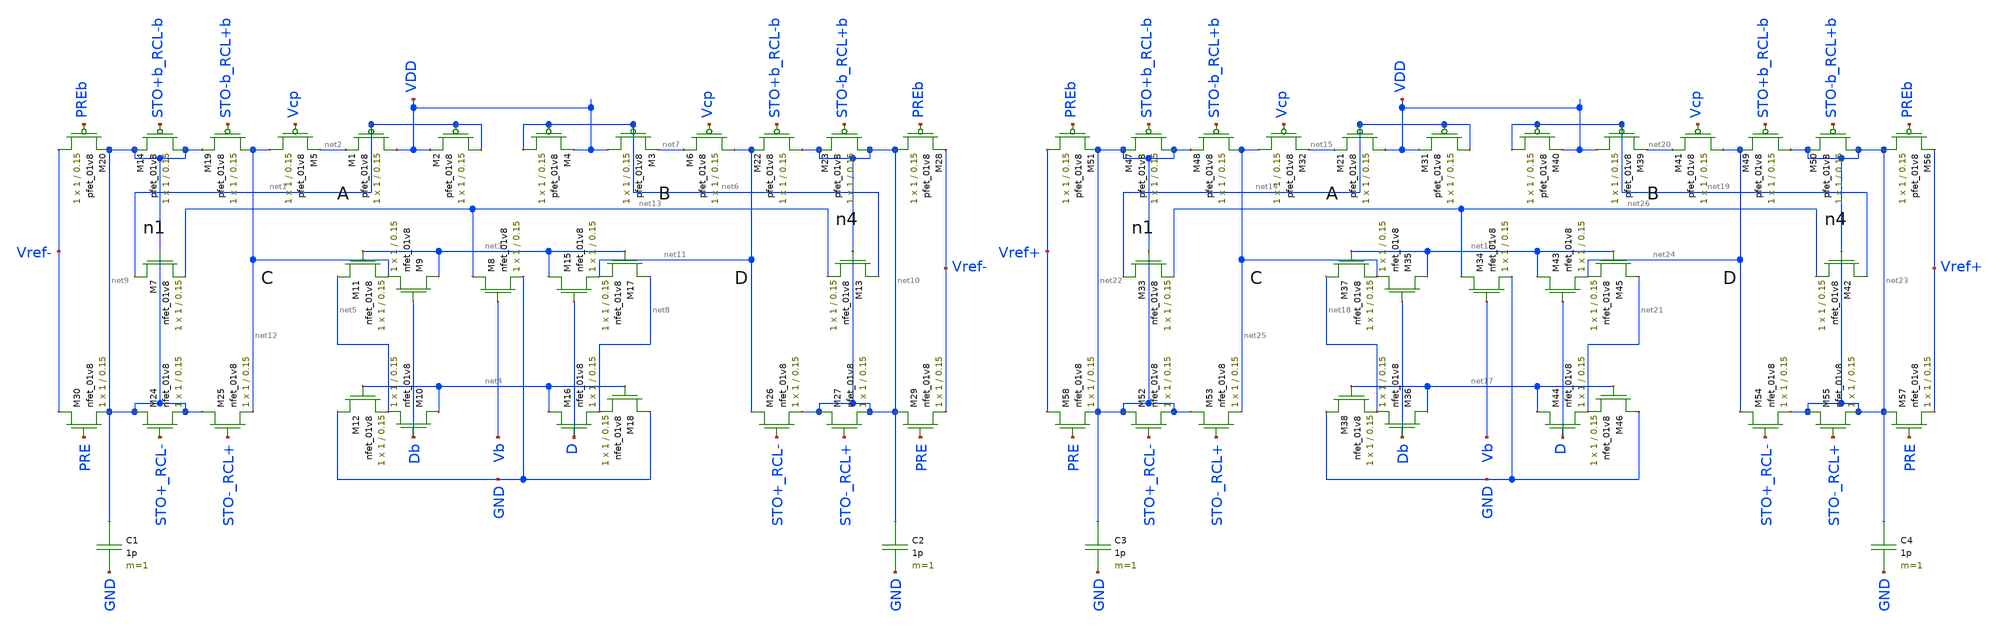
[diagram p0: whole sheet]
** sch_path: OTAs_lds.sch
**.subckt OTAs_lds
XM1 VDD net1 net2 VDD sky130_fd_pr__pfet_01v8 L=0.15 W=1 nf=1 ad='int((nf+1)/2) * W/nf * 0.29' as='int((nf+2)/2) * W/nf * 0.29'
+ pd='2*int((nf+1)/2) * (W/nf + 0.29)' ps='2*int((nf+2)/2) * (W/nf + 0.29)' nrd='0.29 / W' nrs='0.29 / W'
+ sa=0 sb=0 sd=0 mult=1 m=1
XM2 net1 net1 VDD VDD sky130_fd_pr__pfet_01v8 L=0.15 W=1 nf=1 ad='int((nf+1)/2) * W/nf * 0.29' as='int((nf+2)/2) * W/nf * 0.29'
+ pd='2*int((nf+1)/2) * (W/nf + 0.29)' ps='2*int((nf+2)/2) * (W/nf + 0.29)' nrd='0.29 / W' nrs='0.29 / W'
+ sa=0 sb=0 sd=0 mult=1 m=1
XM5 net12 Vcp net2 VDD sky130_fd_pr__pfet_01v8 L=0.15 W=1 nf=1 ad='int((nf+1)/2) * W/nf * 0.29' as='int((nf+2)/2) * W/nf * 0.29'
+ pd='2*int((nf+1)/2) * (W/nf + 0.29)' ps='2*int((nf+2)/2) * (W/nf + 0.29)' nrd='0.29 / W' nrs='0.29 / W'
+ sa=0 sb=0 sd=0 mult=1 m=1
XM7 net1 net9 net13 GND sky130_fd_pr__nfet_01v8 L=0.15 W=1 nf=1 ad='int((nf+1)/2) * W/nf * 0.29' as='int((nf+2)/2) * W/nf * 0.29'
+ pd='2*int((nf+1)/2) * (W/nf + 0.29)' ps='2*int((nf+2)/2) * (W/nf + 0.29)' nrd='0.29 / W' nrs='0.29 / W'
+ sa=0 sb=0 sd=0 mult=1 m=1
XM8 net13 Vb GND GND sky130_fd_pr__nfet_01v8 L=0.15 W=1 nf=1 ad='int((nf+1)/2) * W/nf * 0.29' as='int((nf+2)/2) * W/nf * 0.29'
+ pd='2*int((nf+1)/2) * (W/nf + 0.29)' ps='2*int((nf+2)/2) * (W/nf + 0.29)' nrd='0.29 / W' nrs='0.29 / W'
+ sa=0 sb=0 sd=0 mult=1 m=1
XM9 net3 Db net12 GND sky130_fd_pr__nfet_01v8 L=0.15 W=1 nf=1 ad='int((nf+1)/2) * W/nf * 0.29' as='int((nf+2)/2) * W/nf * 0.29'
+ pd='2*int((nf+1)/2) * (W/nf + 0.29)' ps='2*int((nf+2)/2) * (W/nf + 0.29)' nrd='0.29 / W' nrs='0.29 / W'
+ sa=0 sb=0 sd=0 mult=1 m=1
XM10 net4 Db net5 GND sky130_fd_pr__nfet_01v8 L=0.15 W=1 nf=1 ad='int((nf+1)/2) * W/nf * 0.29' as='int((nf+2)/2) * W/nf * 0.29'
+ pd='2*int((nf+1)/2) * (W/nf + 0.29)' ps='2*int((nf+2)/2) * (W/nf + 0.29)' nrd='0.29 / W' nrs='0.29 / W'
+ sa=0 sb=0 sd=0 mult=1 m=1
XM11 net5 net3 net12 GND sky130_fd_pr__nfet_01v8 L=0.15 W=1 nf=1 ad='int((nf+1)/2) * W/nf * 0.29' as='int((nf+2)/2) * W/nf * 0.29'
+ pd='2*int((nf+1)/2) * (W/nf + 0.29)' ps='2*int((nf+2)/2) * (W/nf + 0.29)' nrd='0.29 / W' nrs='0.29 / W'
+ sa=0 sb=0 sd=0 mult=1 m=1
XM12 GND net4 net5 GND sky130_fd_pr__nfet_01v8 L=0.15 W=1 nf=1 ad='int((nf+1)/2) * W/nf * 0.29' as='int((nf+2)/2) * W/nf * 0.29'
+ pd='2*int((nf+1)/2) * (W/nf + 0.29)' ps='2*int((nf+2)/2) * (W/nf + 0.29)' nrd='0.29 / W' nrs='0.29 / W'
+ sa=0 sb=0 sd=0 mult=1 m=1
XM3 VDD net6 net7 VDD sky130_fd_pr__pfet_01v8 L=0.15 W=1 nf=1 ad='int((nf+1)/2) * W/nf * 0.29' as='int((nf+2)/2) * W/nf * 0.29'
+ pd='2*int((nf+1)/2) * (W/nf + 0.29)' ps='2*int((nf+2)/2) * (W/nf + 0.29)' nrd='0.29 / W' nrs='0.29 / W'
+ sa=0 sb=0 sd=0 mult=1 m=1
XM4 net6 net6 VDD VDD sky130_fd_pr__pfet_01v8 L=0.15 W=1 nf=1 ad='int((nf+1)/2) * W/nf * 0.29' as='int((nf+2)/2) * W/nf * 0.29'
+ pd='2*int((nf+1)/2) * (W/nf + 0.29)' ps='2*int((nf+2)/2) * (W/nf + 0.29)' nrd='0.29 / W' nrs='0.29 / W'
+ sa=0 sb=0 sd=0 mult=1 m=1
XM6 net11 Vcp net7 VDD sky130_fd_pr__pfet_01v8 L=0.15 W=1 nf=1 ad='int((nf+1)/2) * W/nf * 0.29' as='int((nf+2)/2) * W/nf * 0.29'
+ pd='2*int((nf+1)/2) * (W/nf + 0.29)' ps='2*int((nf+2)/2) * (W/nf + 0.29)' nrd='0.29 / W' nrs='0.29 / W'
+ sa=0 sb=0 sd=0 mult=1 m=1
XM13 net6 net10 net13 GND sky130_fd_pr__nfet_01v8 L=0.15 W=1 nf=1 ad='int((nf+1)/2) * W/nf * 0.29' as='int((nf+2)/2) * W/nf * 0.29'
+ pd='2*int((nf+1)/2) * (W/nf + 0.29)' ps='2*int((nf+2)/2) * (W/nf + 0.29)' nrd='0.29 / W' nrs='0.29 / W'
+ sa=0 sb=0 sd=0 mult=1 m=1
XM15 net3 D net11 GND sky130_fd_pr__nfet_01v8 L=0.15 W=1 nf=1 ad='int((nf+1)/2) * W/nf * 0.29' as='int((nf+2)/2) * W/nf * 0.29'
+ pd='2*int((nf+1)/2) * (W/nf + 0.29)' ps='2*int((nf+2)/2) * (W/nf + 0.29)' nrd='0.29 / W' nrs='0.29 / W'
+ sa=0 sb=0 sd=0 mult=1 m=1
XM16 net4 D net8 GND sky130_fd_pr__nfet_01v8 L=0.15 W=1 nf=1 ad='int((nf+1)/2) * W/nf * 0.29' as='int((nf+2)/2) * W/nf * 0.29'
+ pd='2*int((nf+1)/2) * (W/nf + 0.29)' ps='2*int((nf+2)/2) * (W/nf + 0.29)' nrd='0.29 / W' nrs='0.29 / W'
+ sa=0 sb=0 sd=0 mult=1 m=1
XM17 net8 net3 net11 GND sky130_fd_pr__nfet_01v8 L=0.15 W=1 nf=1 ad='int((nf+1)/2) * W/nf * 0.29' as='int((nf+2)/2) * W/nf * 0.29'
+ pd='2*int((nf+1)/2) * (W/nf + 0.29)' ps='2*int((nf+2)/2) * (W/nf + 0.29)' nrd='0.29 / W' nrs='0.29 / W'
+ sa=0 sb=0 sd=0 mult=1 m=1
XM18 GND net4 net8 GND sky130_fd_pr__nfet_01v8 L=0.15 W=1 nf=1 ad='int((nf+1)/2) * W/nf * 0.29' as='int((nf+2)/2) * W/nf * 0.29'
+ pd='2*int((nf+1)/2) * (W/nf + 0.29)' ps='2*int((nf+2)/2) * (W/nf + 0.29)' nrd='0.29 / W' nrs='0.29 / W'
+ sa=0 sb=0 sd=0 mult=1 m=1
XM14 net9 STO+b_RCL-b net9 VDD sky130_fd_pr__pfet_01v8 L=0.15 W=1 nf=1 ad='int((nf+1)/2) * W/nf * 0.29'
+ as='int((nf+2)/2) * W/nf * 0.29' pd='2*int((nf+1)/2) * (W/nf + 0.29)' ps='2*int((nf+2)/2) * (W/nf + 0.29)'
+ nrd='0.29 / W' nrs='0.29 / W' sa=0 sb=0 sd=0 mult=1 m=1
XM19 net12 STO-b_RCL+b net9 VDD sky130_fd_pr__pfet_01v8 L=0.15 W=1 nf=1 ad='int((nf+1)/2) * W/nf * 0.29'
+ as='int((nf+2)/2) * W/nf * 0.29' pd='2*int((nf+1)/2) * (W/nf + 0.29)' ps='2*int((nf+2)/2) * (W/nf + 0.29)'
+ nrd='0.29 / W' nrs='0.29 / W' sa=0 sb=0 sd=0 mult=1 m=1
XM22 net10 STO+b_RCL-b net11 VDD sky130_fd_pr__pfet_01v8 L=0.15 W=1 nf=1 ad='int((nf+1)/2) * W/nf * 0.29'
+ as='int((nf+2)/2) * W/nf * 0.29' pd='2*int((nf+1)/2) * (W/nf + 0.29)' ps='2*int((nf+2)/2) * (W/nf + 0.29)'
+ nrd='0.29 / W' nrs='0.29 / W' sa=0 sb=0 sd=0 mult=1 m=1
XM23 net10 STO-b_RCL+b net10 VDD sky130_fd_pr__pfet_01v8 L=0.15 W=1 nf=1 ad='int((nf+1)/2) * W/nf * 0.29'
+ as='int((nf+2)/2) * W/nf * 0.29' pd='2*int((nf+1)/2) * (W/nf + 0.29)' ps='2*int((nf+2)/2) * (W/nf + 0.29)'
+ nrd='0.29 / W' nrs='0.29 / W' sa=0 sb=0 sd=0 mult=1 m=1
XM20 Vref- PREb net9 VDD sky130_fd_pr__pfet_01v8 L=0.15 W=1 nf=1 ad='int((nf+1)/2) * W/nf * 0.29' as='int((nf+2)/2) * W/nf * 0.29'
+ pd='2*int((nf+1)/2) * (W/nf + 0.29)' ps='2*int((nf+2)/2) * (W/nf + 0.29)' nrd='0.29 / W' nrs='0.29 / W'
+ sa=0 sb=0 sd=0 mult=1 m=1
XM24 net9 STO+_RCL- net9 GND sky130_fd_pr__nfet_01v8 L=0.15 W=1 nf=1 ad='int((nf+1)/2) * W/nf * 0.29'
+ as='int((nf+2)/2) * W/nf * 0.29' pd='2*int((nf+1)/2) * (W/nf + 0.29)' ps='2*int((nf+2)/2) * (W/nf + 0.29)'
+ nrd='0.29 / W' nrs='0.29 / W' sa=0 sb=0 sd=0 mult=1 m=1
XM25 net9 STO-_RCL+ net12 GND sky130_fd_pr__nfet_01v8 L=0.15 W=1 nf=1 ad='int((nf+1)/2) * W/nf * 0.29'
+ as='int((nf+2)/2) * W/nf * 0.29' pd='2*int((nf+1)/2) * (W/nf + 0.29)' ps='2*int((nf+2)/2) * (W/nf + 0.29)'
+ nrd='0.29 / W' nrs='0.29 / W' sa=0 sb=0 sd=0 mult=1 m=1
XM26 net11 STO+_RCL- net10 GND sky130_fd_pr__nfet_01v8 L=0.15 W=1 nf=1 ad='int((nf+1)/2) * W/nf * 0.29'
+ as='int((nf+2)/2) * W/nf * 0.29' pd='2*int((nf+1)/2) * (W/nf + 0.29)' ps='2*int((nf+2)/2) * (W/nf + 0.29)'
+ nrd='0.29 / W' nrs='0.29 / W' sa=0 sb=0 sd=0 mult=1 m=1
XM27 net10 STO-_RCL+ net10 GND sky130_fd_pr__nfet_01v8 L=0.15 W=1 nf=1 ad='int((nf+1)/2) * W/nf * 0.29'
+ as='int((nf+2)/2) * W/nf * 0.29' pd='2*int((nf+1)/2) * (W/nf + 0.29)' ps='2*int((nf+2)/2) * (W/nf + 0.29)'
+ nrd='0.29 / W' nrs='0.29 / W' sa=0 sb=0 sd=0 mult=1 m=1
XM28 net10 PREb Vref- VDD sky130_fd_pr__pfet_01v8 L=0.15 W=1 nf=1 ad='int((nf+1)/2) * W/nf * 0.29' as='int((nf+2)/2) * W/nf * 0.29'
+ pd='2*int((nf+1)/2) * (W/nf + 0.29)' ps='2*int((nf+2)/2) * (W/nf + 0.29)' nrd='0.29 / W' nrs='0.29 / W'
+ sa=0 sb=0 sd=0 mult=1 m=1
XM29 net10 PRE Vref- GND sky130_fd_pr__nfet_01v8 L=0.15 W=1 nf=1 ad='int((nf+1)/2) * W/nf * 0.29' as='int((nf+2)/2) * W/nf * 0.29'
+ pd='2*int((nf+1)/2) * (W/nf + 0.29)' ps='2*int((nf+2)/2) * (W/nf + 0.29)' nrd='0.29 / W' nrs='0.29 / W'
+ sa=0 sb=0 sd=0 mult=1 m=1
XM30 Vref- PRE net9 GND sky130_fd_pr__nfet_01v8 L=0.15 W=1 nf=1 ad='int((nf+1)/2) * W/nf * 0.29' as='int((nf+2)/2) * W/nf * 0.29'
+ pd='2*int((nf+1)/2) * (W/nf + 0.29)' ps='2*int((nf+2)/2) * (W/nf + 0.29)' nrd='0.29 / W' nrs='0.29 / W'
+ sa=0 sb=0 sd=0 mult=1 m=1
C1 net9 GND 1p m=1
C2 net10 GND 1p m=1
XM21 VDD net14 net15 VDD sky130_fd_pr__pfet_01v8 L=0.15 W=1 nf=1 ad='int((nf+1)/2) * W/nf * 0.29' as='int((nf+2)/2) * W/nf * 0.29'
+ pd='2*int((nf+1)/2) * (W/nf + 0.29)' ps='2*int((nf+2)/2) * (W/nf + 0.29)' nrd='0.29 / W' nrs='0.29 / W'
+ sa=0 sb=0 sd=0 mult=1 m=1
XM31 net14 net14 VDD VDD sky130_fd_pr__pfet_01v8 L=0.15 W=1 nf=1 ad='int((nf+1)/2) * W/nf * 0.29' as='int((nf+2)/2) * W/nf * 0.29'
+ pd='2*int((nf+1)/2) * (W/nf + 0.29)' ps='2*int((nf+2)/2) * (W/nf + 0.29)' nrd='0.29 / W' nrs='0.29 / W'
+ sa=0 sb=0 sd=0 mult=1 m=1
XM32 net25 Vcp net15 VDD sky130_fd_pr__pfet_01v8 L=0.15 W=1 nf=1 ad='int((nf+1)/2) * W/nf * 0.29' as='int((nf+2)/2) * W/nf * 0.29'
+ pd='2*int((nf+1)/2) * (W/nf + 0.29)' ps='2*int((nf+2)/2) * (W/nf + 0.29)' nrd='0.29 / W' nrs='0.29 / W'
+ sa=0 sb=0 sd=0 mult=1 m=1
XM33 net14 net22 net26 GND sky130_fd_pr__nfet_01v8 L=0.15 W=1 nf=1 ad='int((nf+1)/2) * W/nf * 0.29' as='int((nf+2)/2) * W/nf * 0.29'
+ pd='2*int((nf+1)/2) * (W/nf + 0.29)' ps='2*int((nf+2)/2) * (W/nf + 0.29)' nrd='0.29 / W' nrs='0.29 / W'
+ sa=0 sb=0 sd=0 mult=1 m=1
XM34 net26 Vb GND GND sky130_fd_pr__nfet_01v8 L=0.15 W=1 nf=1 ad='int((nf+1)/2) * W/nf * 0.29' as='int((nf+2)/2) * W/nf * 0.29'
+ pd='2*int((nf+1)/2) * (W/nf + 0.29)' ps='2*int((nf+2)/2) * (W/nf + 0.29)' nrd='0.29 / W' nrs='0.29 / W'
+ sa=0 sb=0 sd=0 mult=1 m=1
XM35 net16 Db net25 GND sky130_fd_pr__nfet_01v8 L=0.15 W=1 nf=1 ad='int((nf+1)/2) * W/nf * 0.29' as='int((nf+2)/2) * W/nf * 0.29'
+ pd='2*int((nf+1)/2) * (W/nf + 0.29)' ps='2*int((nf+2)/2) * (W/nf + 0.29)' nrd='0.29 / W' nrs='0.29 / W'
+ sa=0 sb=0 sd=0 mult=1 m=1
XM36 net17 Db net18 GND sky130_fd_pr__nfet_01v8 L=0.15 W=1 nf=1 ad='int((nf+1)/2) * W/nf * 0.29' as='int((nf+2)/2) * W/nf * 0.29'
+ pd='2*int((nf+1)/2) * (W/nf + 0.29)' ps='2*int((nf+2)/2) * (W/nf + 0.29)' nrd='0.29 / W' nrs='0.29 / W'
+ sa=0 sb=0 sd=0 mult=1 m=1
XM37 net18 net16 net25 GND sky130_fd_pr__nfet_01v8 L=0.15 W=1 nf=1 ad='int((nf+1)/2) * W/nf * 0.29' as='int((nf+2)/2) * W/nf * 0.29'
+ pd='2*int((nf+1)/2) * (W/nf + 0.29)' ps='2*int((nf+2)/2) * (W/nf + 0.29)' nrd='0.29 / W' nrs='0.29 / W'
+ sa=0 sb=0 sd=0 mult=1 m=1
XM38 GND net17 net18 GND sky130_fd_pr__nfet_01v8 L=0.15 W=1 nf=1 ad='int((nf+1)/2) * W/nf * 0.29' as='int((nf+2)/2) * W/nf * 0.29'
+ pd='2*int((nf+1)/2) * (W/nf + 0.29)' ps='2*int((nf+2)/2) * (W/nf + 0.29)' nrd='0.29 / W' nrs='0.29 / W'
+ sa=0 sb=0 sd=0 mult=1 m=1
XM39 VDD net19 net20 VDD sky130_fd_pr__pfet_01v8 L=0.15 W=1 nf=1 ad='int((nf+1)/2) * W/nf * 0.29' as='int((nf+2)/2) * W/nf * 0.29'
+ pd='2*int((nf+1)/2) * (W/nf + 0.29)' ps='2*int((nf+2)/2) * (W/nf + 0.29)' nrd='0.29 / W' nrs='0.29 / W'
+ sa=0 sb=0 sd=0 mult=1 m=1
XM40 net19 net19 VDD VDD sky130_fd_pr__pfet_01v8 L=0.15 W=1 nf=1 ad='int((nf+1)/2) * W/nf * 0.29' as='int((nf+2)/2) * W/nf * 0.29'
+ pd='2*int((nf+1)/2) * (W/nf + 0.29)' ps='2*int((nf+2)/2) * (W/nf + 0.29)' nrd='0.29 / W' nrs='0.29 / W'
+ sa=0 sb=0 sd=0 mult=1 m=1
XM41 net24 Vcp net20 VDD sky130_fd_pr__pfet_01v8 L=0.15 W=1 nf=1 ad='int((nf+1)/2) * W/nf * 0.29' as='int((nf+2)/2) * W/nf * 0.29'
+ pd='2*int((nf+1)/2) * (W/nf + 0.29)' ps='2*int((nf+2)/2) * (W/nf + 0.29)' nrd='0.29 / W' nrs='0.29 / W'
+ sa=0 sb=0 sd=0 mult=1 m=1
XM42 net19 net23 net26 GND sky130_fd_pr__nfet_01v8 L=0.15 W=1 nf=1 ad='int((nf+1)/2) * W/nf * 0.29' as='int((nf+2)/2) * W/nf * 0.29'
+ pd='2*int((nf+1)/2) * (W/nf + 0.29)' ps='2*int((nf+2)/2) * (W/nf + 0.29)' nrd='0.29 / W' nrs='0.29 / W'
+ sa=0 sb=0 sd=0 mult=1 m=1
XM43 net16 D net24 GND sky130_fd_pr__nfet_01v8 L=0.15 W=1 nf=1 ad='int((nf+1)/2) * W/nf * 0.29' as='int((nf+2)/2) * W/nf * 0.29'
+ pd='2*int((nf+1)/2) * (W/nf + 0.29)' ps='2*int((nf+2)/2) * (W/nf + 0.29)' nrd='0.29 / W' nrs='0.29 / W'
+ sa=0 sb=0 sd=0 mult=1 m=1
XM44 net17 D net21 GND sky130_fd_pr__nfet_01v8 L=0.15 W=1 nf=1 ad='int((nf+1)/2) * W/nf * 0.29' as='int((nf+2)/2) * W/nf * 0.29'
+ pd='2*int((nf+1)/2) * (W/nf + 0.29)' ps='2*int((nf+2)/2) * (W/nf + 0.29)' nrd='0.29 / W' nrs='0.29 / W'
+ sa=0 sb=0 sd=0 mult=1 m=1
XM45 net21 net16 net24 GND sky130_fd_pr__nfet_01v8 L=0.15 W=1 nf=1 ad='int((nf+1)/2) * W/nf * 0.29' as='int((nf+2)/2) * W/nf * 0.29'
+ pd='2*int((nf+1)/2) * (W/nf + 0.29)' ps='2*int((nf+2)/2) * (W/nf + 0.29)' nrd='0.29 / W' nrs='0.29 / W'
+ sa=0 sb=0 sd=0 mult=1 m=1
XM46 GND net17 net21 GND sky130_fd_pr__nfet_01v8 L=0.15 W=1 nf=1 ad='int((nf+1)/2) * W/nf * 0.29' as='int((nf+2)/2) * W/nf * 0.29'
+ pd='2*int((nf+1)/2) * (W/nf + 0.29)' ps='2*int((nf+2)/2) * (W/nf + 0.29)' nrd='0.29 / W' nrs='0.29 / W'
+ sa=0 sb=0 sd=0 mult=1 m=1
XM47 net22 STO+b_RCL-b net22 VDD sky130_fd_pr__pfet_01v8 L=0.15 W=1 nf=1 ad='int((nf+1)/2) * W/nf * 0.29'
+ as='int((nf+2)/2) * W/nf * 0.29' pd='2*int((nf+1)/2) * (W/nf + 0.29)' ps='2*int((nf+2)/2) * (W/nf + 0.29)'
+ nrd='0.29 / W' nrs='0.29 / W' sa=0 sb=0 sd=0 mult=1 m=1
XM48 net25 STO-b_RCL+b net22 VDD sky130_fd_pr__pfet_01v8 L=0.15 W=1 nf=1 ad='int((nf+1)/2) * W/nf * 0.29'
+ as='int((nf+2)/2) * W/nf * 0.29' pd='2*int((nf+1)/2) * (W/nf + 0.29)' ps='2*int((nf+2)/2) * (W/nf + 0.29)'
+ nrd='0.29 / W' nrs='0.29 / W' sa=0 sb=0 sd=0 mult=1 m=1
XM49 net23 STO+b_RCL-b net24 VDD sky130_fd_pr__pfet_01v8 L=0.15 W=1 nf=1 ad='int((nf+1)/2) * W/nf * 0.29'
+ as='int((nf+2)/2) * W/nf * 0.29' pd='2*int((nf+1)/2) * (W/nf + 0.29)' ps='2*int((nf+2)/2) * (W/nf + 0.29)'
+ nrd='0.29 / W' nrs='0.29 / W' sa=0 sb=0 sd=0 mult=1 m=1
XM50 net23 STO-b_RCL+b net23 VDD sky130_fd_pr__pfet_01v8 L=0.15 W=1 nf=1 ad='int((nf+1)/2) * W/nf * 0.29'
+ as='int((nf+2)/2) * W/nf * 0.29' pd='2*int((nf+1)/2) * (W/nf + 0.29)' ps='2*int((nf+2)/2) * (W/nf + 0.29)'
+ nrd='0.29 / W' nrs='0.29 / W' sa=0 sb=0 sd=0 mult=1 m=1
XM51 Vref+ PREb net22 VDD sky130_fd_pr__pfet_01v8 L=0.15 W=1 nf=1 ad='int((nf+1)/2) * W/nf * 0.29' as='int((nf+2)/2) * W/nf * 0.29'
+ pd='2*int((nf+1)/2) * (W/nf + 0.29)' ps='2*int((nf+2)/2) * (W/nf + 0.29)' nrd='0.29 / W' nrs='0.29 / W'
+ sa=0 sb=0 sd=0 mult=1 m=1
XM52 net22 STO+_RCL- net22 GND sky130_fd_pr__nfet_01v8 L=0.15 W=1 nf=1 ad='int((nf+1)/2) * W/nf * 0.29'
+ as='int((nf+2)/2) * W/nf * 0.29' pd='2*int((nf+1)/2) * (W/nf + 0.29)' ps='2*int((nf+2)/2) * (W/nf + 0.29)'
+ nrd='0.29 / W' nrs='0.29 / W' sa=0 sb=0 sd=0 mult=1 m=1
XM53 net22 STO-_RCL+ net25 GND sky130_fd_pr__nfet_01v8 L=0.15 W=1 nf=1 ad='int((nf+1)/2) * W/nf * 0.29'
+ as='int((nf+2)/2) * W/nf * 0.29' pd='2*int((nf+1)/2) * (W/nf + 0.29)' ps='2*int((nf+2)/2) * (W/nf + 0.29)'
+ nrd='0.29 / W' nrs='0.29 / W' sa=0 sb=0 sd=0 mult=1 m=1
XM54 net24 STO+_RCL- net23 GND sky130_fd_pr__nfet_01v8 L=0.15 W=1 nf=1 ad='int((nf+1)/2) * W/nf * 0.29'
+ as='int((nf+2)/2) * W/nf * 0.29' pd='2*int((nf+1)/2) * (W/nf + 0.29)' ps='2*int((nf+2)/2) * (W/nf + 0.29)'
+ nrd='0.29 / W' nrs='0.29 / W' sa=0 sb=0 sd=0 mult=1 m=1
XM55 net23 STO-_RCL+ net23 GND sky130_fd_pr__nfet_01v8 L=0.15 W=1 nf=1 ad='int((nf+1)/2) * W/nf * 0.29'
+ as='int((nf+2)/2) * W/nf * 0.29' pd='2*int((nf+1)/2) * (W/nf + 0.29)' ps='2*int((nf+2)/2) * (W/nf + 0.29)'
+ nrd='0.29 / W' nrs='0.29 / W' sa=0 sb=0 sd=0 mult=1 m=1
XM56 net23 PREb Vref+ VDD sky130_fd_pr__pfet_01v8 L=0.15 W=1 nf=1 ad='int((nf+1)/2) * W/nf * 0.29' as='int((nf+2)/2) * W/nf * 0.29'
+ pd='2*int((nf+1)/2) * (W/nf + 0.29)' ps='2*int((nf+2)/2) * (W/nf + 0.29)' nrd='0.29 / W' nrs='0.29 / W'
+ sa=0 sb=0 sd=0 mult=1 m=1
XM57 net23 PRE Vref+ GND sky130_fd_pr__nfet_01v8 L=0.15 W=1 nf=1 ad='int((nf+1)/2) * W/nf * 0.29' as='int((nf+2)/2) * W/nf * 0.29'
+ pd='2*int((nf+1)/2) * (W/nf + 0.29)' ps='2*int((nf+2)/2) * (W/nf + 0.29)' nrd='0.29 / W' nrs='0.29 / W'
+ sa=0 sb=0 sd=0 mult=1 m=1
XM58 Vref+ PRE net22 GND sky130_fd_pr__nfet_01v8 L=0.15 W=1 nf=1 ad='int((nf+1)/2) * W/nf * 0.29' as='int((nf+2)/2) * W/nf * 0.29'
+ pd='2*int((nf+1)/2) * (W/nf + 0.29)' ps='2*int((nf+2)/2) * (W/nf + 0.29)' nrd='0.29 / W' nrs='0.29 / W'
+ sa=0 sb=0 sd=0 mult=1 m=1
C3 net22 GND 1p m=1
C4 net23 GND 1p m=1
**.ends
.end
